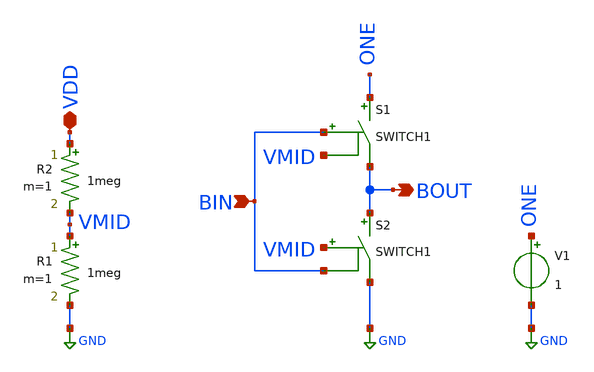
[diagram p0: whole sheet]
** sch_path: XSCHEM Files/Bitlogic.sch
**.subckt Bitlogic BOUT BIN VDD
*.opin BOUT
*.ipin BIN
*.iopin VDD
V1 ONE GND 1
S1 ONE BOUT BIN VMID SWITCH1
S2 BOUT GND VMID BIN SWITCH1
R1 VMID GND 1meg m=1
R2 VDD VMID 1meg m=1
**.ends
.GLOBAL GND
.end
